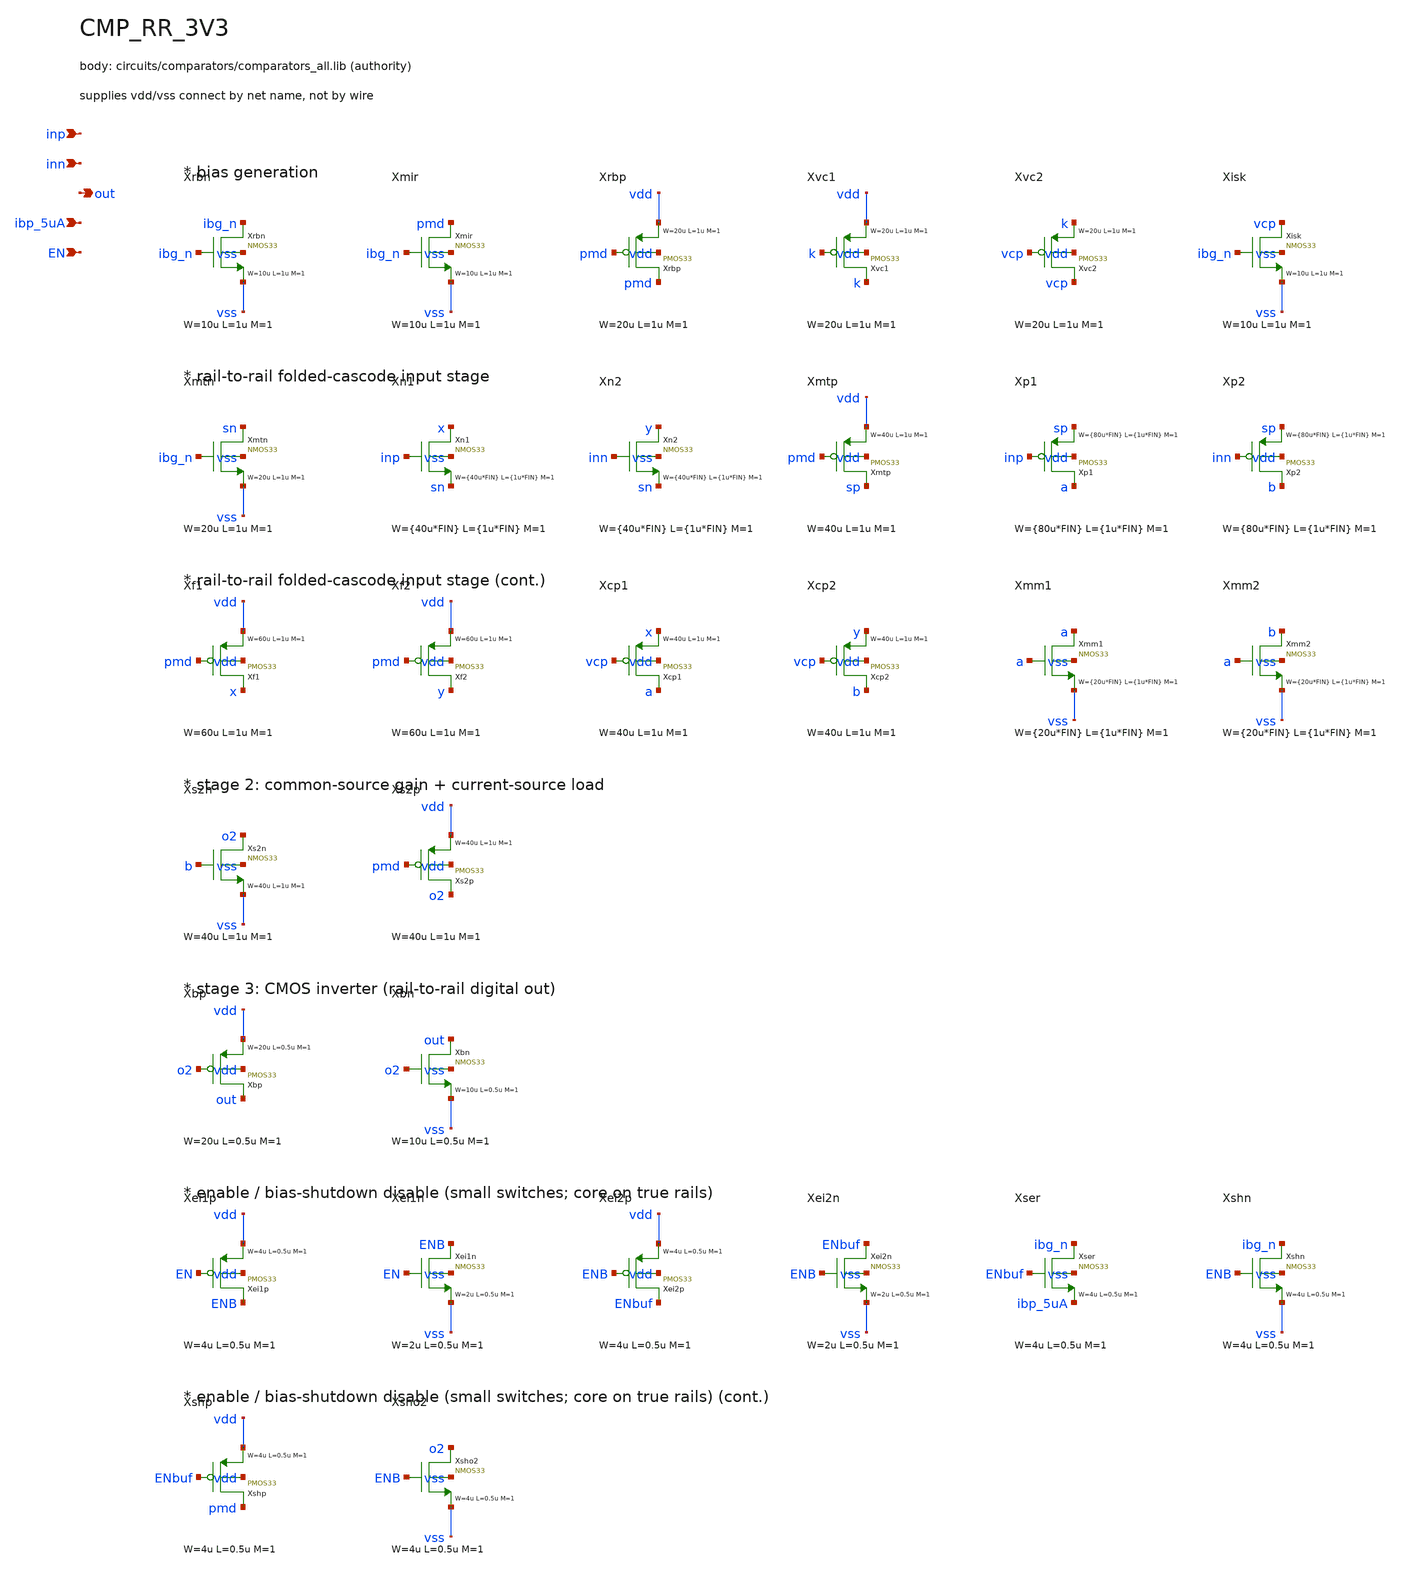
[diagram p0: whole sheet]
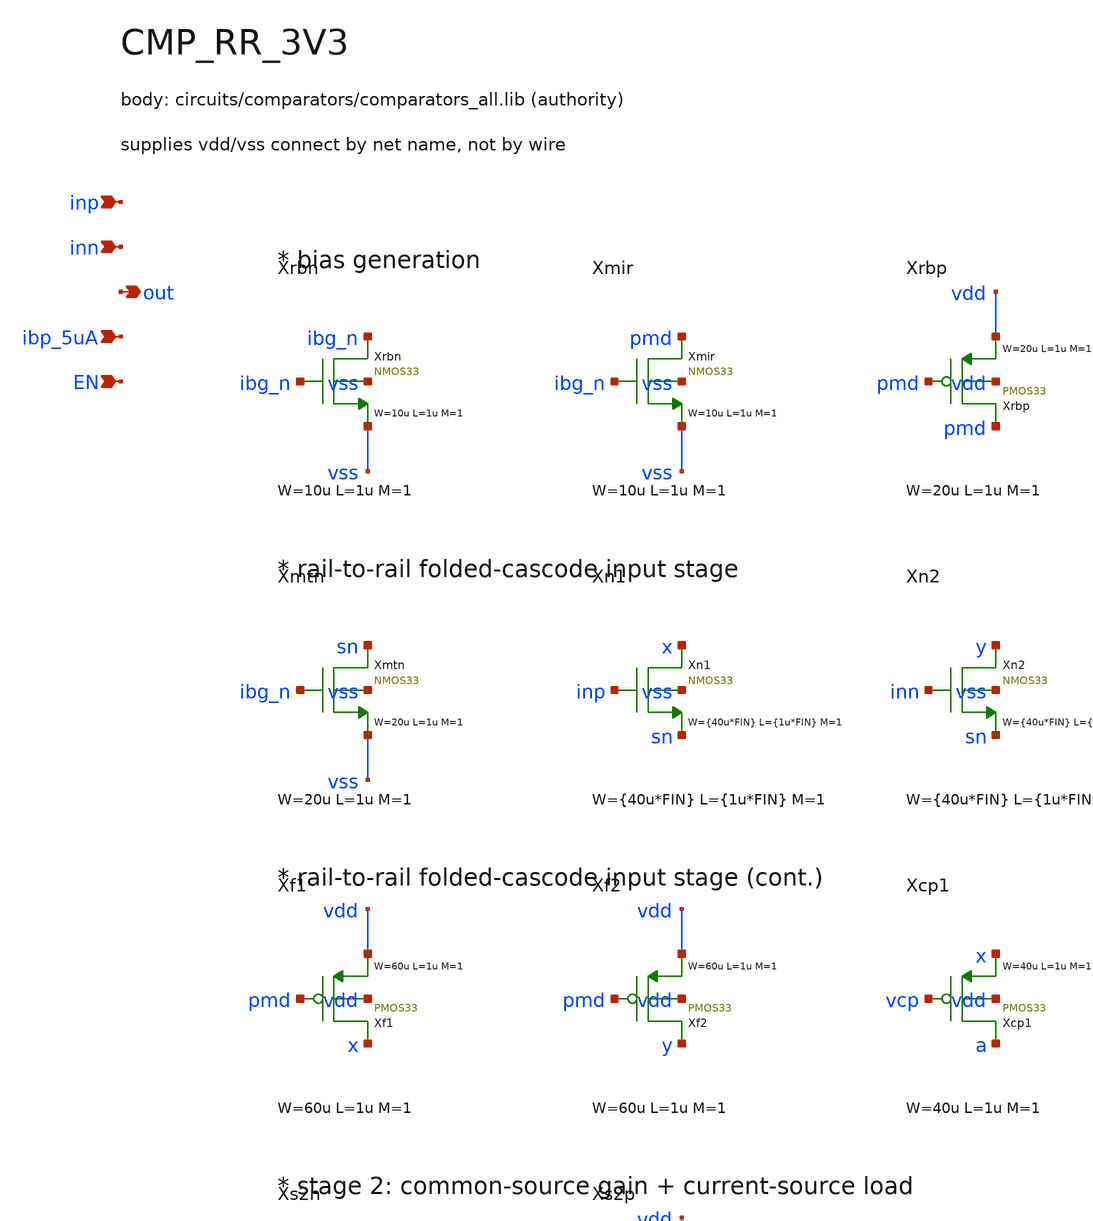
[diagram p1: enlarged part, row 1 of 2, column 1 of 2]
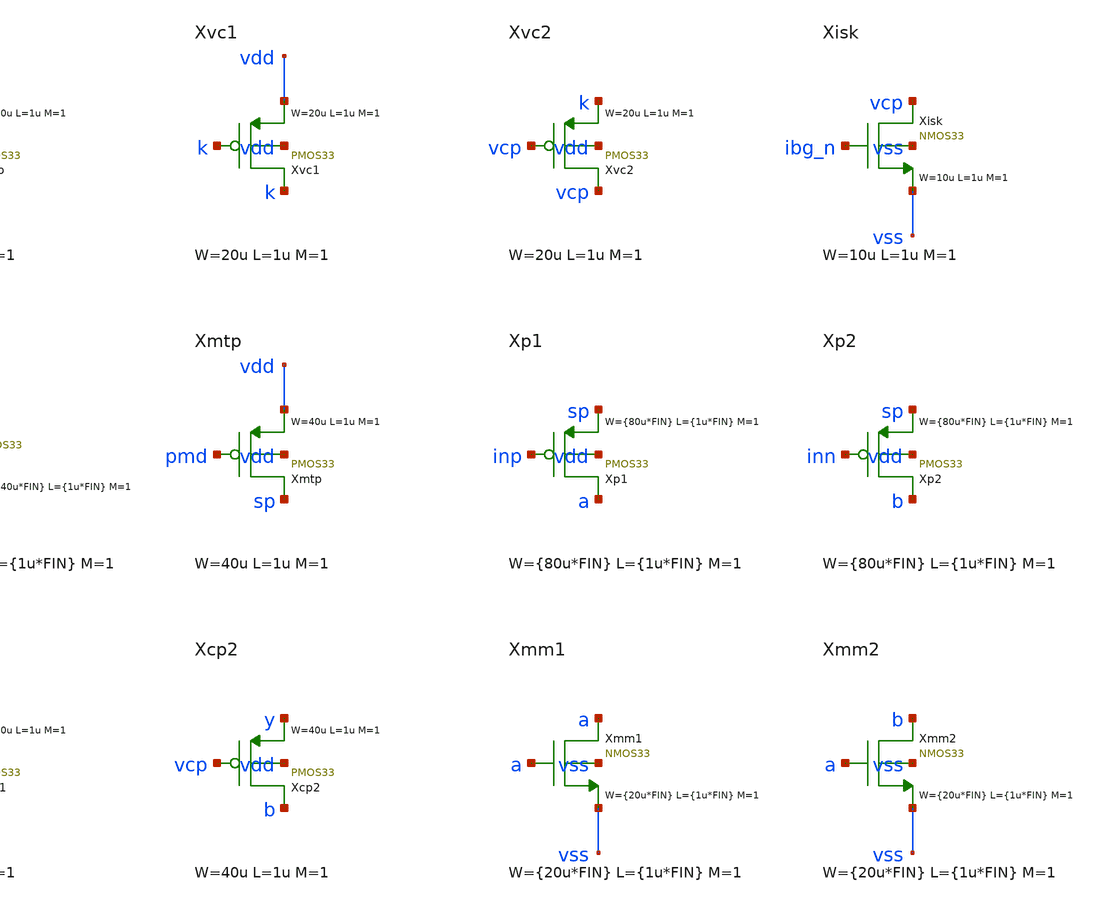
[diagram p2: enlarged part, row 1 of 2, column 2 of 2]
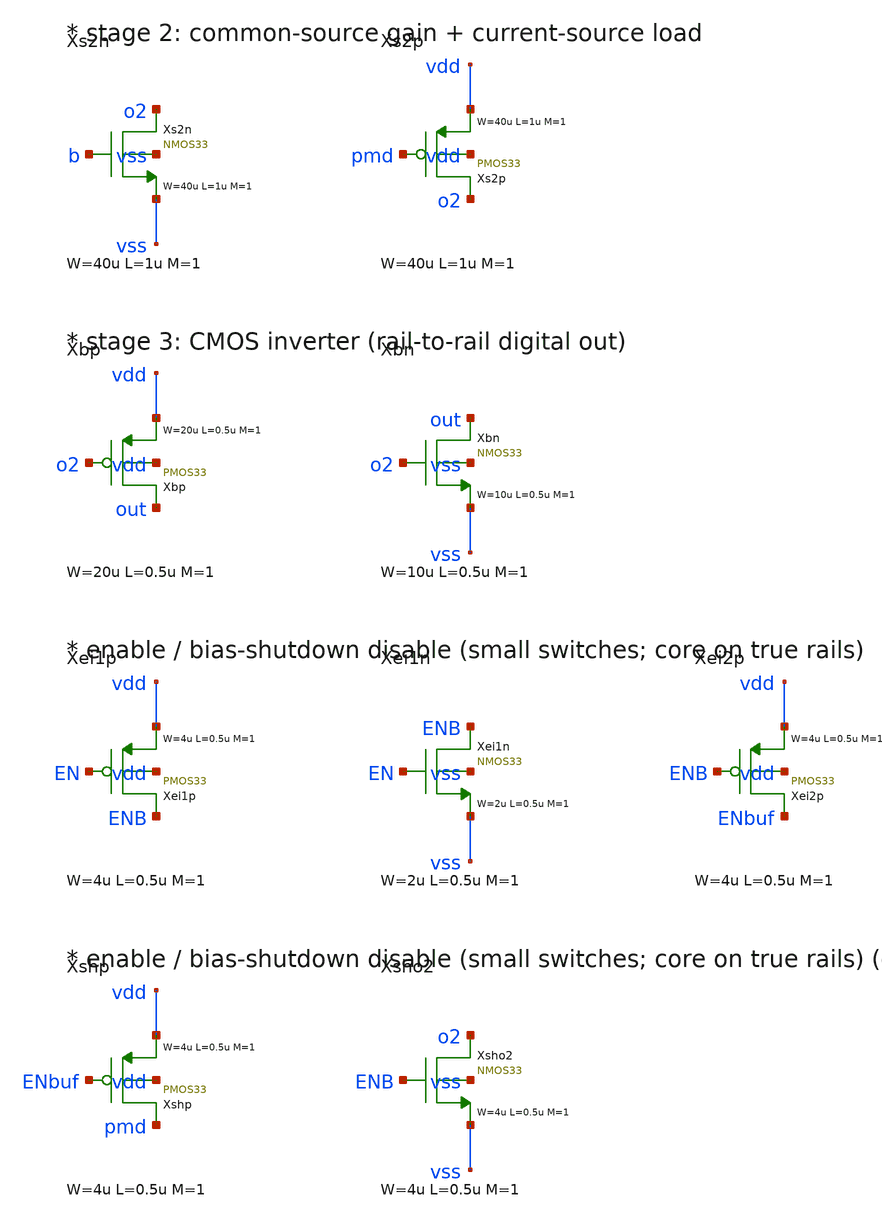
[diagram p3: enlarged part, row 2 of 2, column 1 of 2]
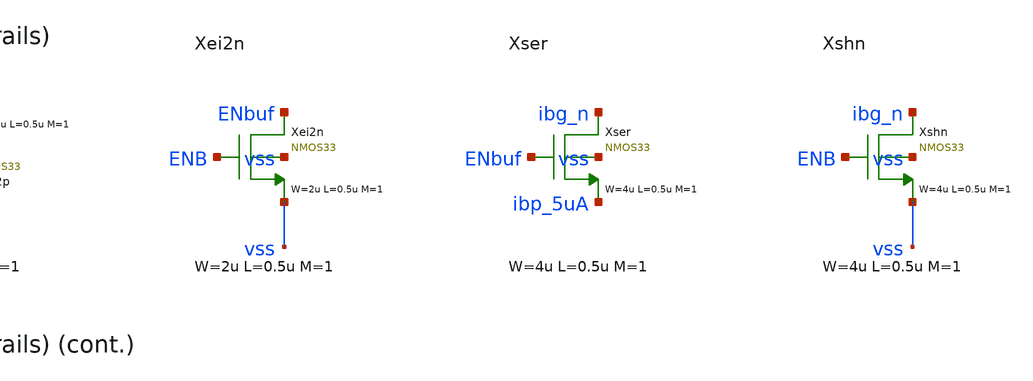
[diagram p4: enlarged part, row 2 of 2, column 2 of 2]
** sch_path: xschem/comparators/CMP_RR_3V3.sch
**.subckt CMP_RR_3V3 inp inn out ibp_5uA EN
*.ipin inp
*.ipin inn
*.opin out
*.ipin ibp_5uA
*.ipin EN
Xrbn ibg_n ibg_n vss vss NMOS33 W=10u L=1u M=1 MM_SIGMA=0
Xmir pmd ibg_n vss vss NMOS33 W=10u L=1u M=1 MM_SIGMA=0
Xrbp pmd pmd vdd vdd PMOS33 W=20u L=1u M=1 MM_SIGMA=0
Xvc1 k k vdd vdd PMOS33 W=20u L=1u M=1 MM_SIGMA=0
Xvc2 vcp vcp k vdd PMOS33 W=20u L=1u M=1 MM_SIGMA=0
Xisk vcp ibg_n vss vss NMOS33 W=10u L=1u M=1 MM_SIGMA=0
Xmtn sn ibg_n vss vss NMOS33 W=20u L=1u M=1 MM_SIGMA=0
Xn1 x inp sn vss NMOS33 W={40u*FIN} L={1u*FIN} M=1 MM_SIGMA=0
Xn2 y inn sn vss NMOS33 W={40u*FIN} L={1u*FIN} M=1 MM_SIGMA=0
Xmtp sp pmd vdd vdd PMOS33 W=40u L=1u M=1 MM_SIGMA=0
Xp1 a inp sp vdd PMOS33 W={80u*FIN} L={1u*FIN} M=1 MM_SIGMA=0
Xp2 b inn sp vdd PMOS33 W={80u*FIN} L={1u*FIN} M=1 MM_SIGMA=0
Xf1 x pmd vdd vdd PMOS33 W=60u L=1u M=1 MM_SIGMA=0
Xf2 y pmd vdd vdd PMOS33 W=60u L=1u M=1 MM_SIGMA=0
Xcp1 a vcp x vdd PMOS33 W=40u L=1u M=1 MM_SIGMA=0
Xcp2 b vcp y vdd PMOS33 W=40u L=1u M=1 MM_SIGMA=0
Xmm1 a a vss vss NMOS33 W={20u*FIN} L={1u*FIN} M=1 MM_SIGMA=0
Xmm2 b a vss vss NMOS33 W={20u*FIN} L={1u*FIN} M=1 MM_SIGMA=0
Xs2n o2 b vss vss NMOS33 W=40u L=1u M=1 MM_SIGMA=0
Xs2p o2 pmd vdd vdd PMOS33 W=40u L=1u M=1 MM_SIGMA=0
Xbp out o2 vdd vdd PMOS33 W=20u L=0.5u M=1 MM_SIGMA=0
Xbn out o2 vss vss NMOS33 W=10u L=0.5u M=1 MM_SIGMA=0
Xei1p ENB EN vdd vdd PMOS33 W=4u L=0.5u M=1 MM_SIGMA=0
Xei1n ENB EN vss vss NMOS33 W=2u L=0.5u M=1 MM_SIGMA=0
Xei2p ENbuf ENB vdd vdd PMOS33 W=4u L=0.5u M=1 MM_SIGMA=0
Xei2n ENbuf ENB vss vss NMOS33 W=2u L=0.5u M=1 MM_SIGMA=0
Xser ibg_n ENbuf ibp_5uA vss NMOS33 W=4u L=0.5u M=1 MM_SIGMA=0
Xshn ibg_n ENB vss vss NMOS33 W=4u L=0.5u M=1 MM_SIGMA=0
Xshp pmd ENbuf vdd vdd PMOS33 W=4u L=0.5u M=1 MM_SIGMA=0
Xsho2 o2 ENB vss vss NMOS33 W=4u L=0.5u M=1 MM_SIGMA=0
**.ends
.end
